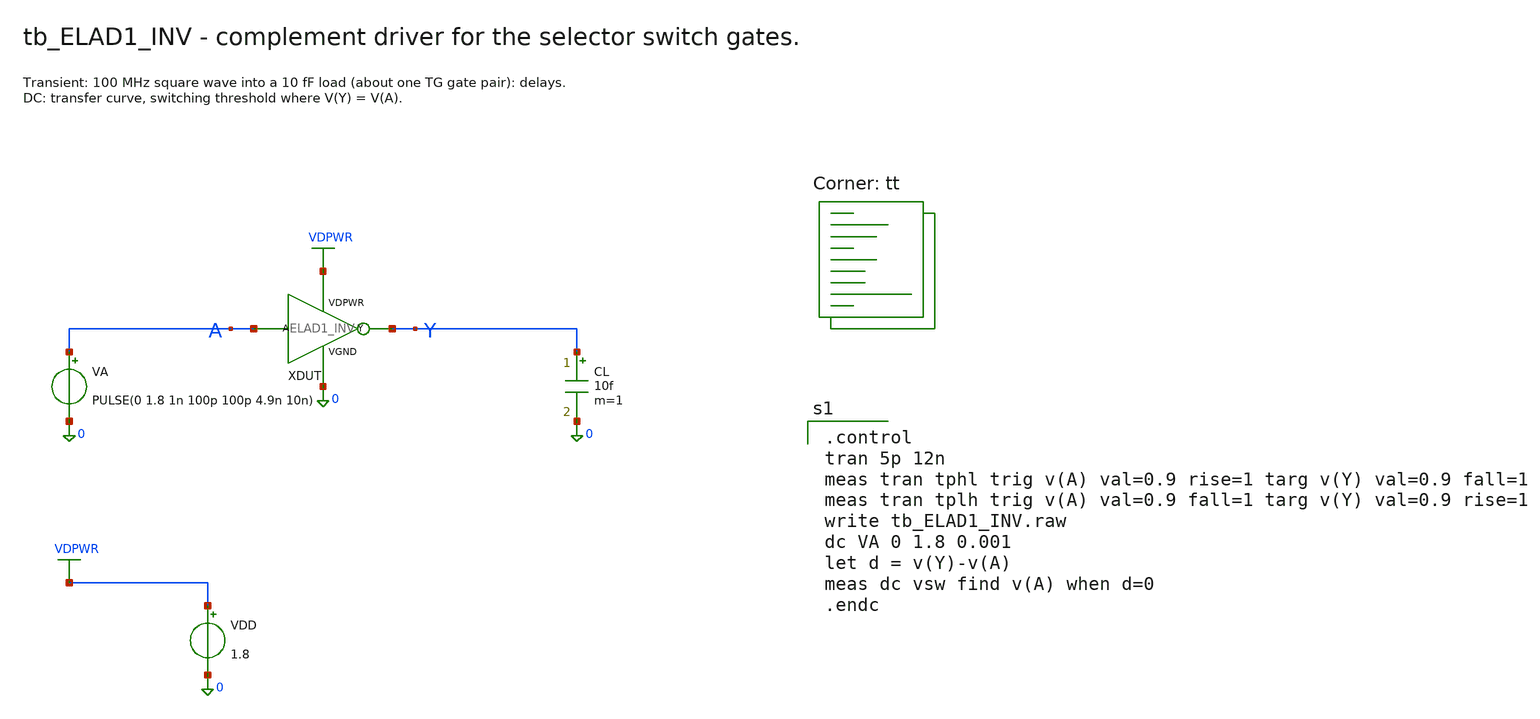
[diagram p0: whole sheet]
** sch_path: cells/ELAD1_INV/schematic/tb_ELAD1_INV.sch
**.subckt tb_ELAD1_INV
XDUT A Y VDPWR 0 ELAD1_INV
VA A 0 PULSE(0 1.8 1n 100p 100p 4.9n 10n)
CL Y 0 10f m=1
VDD VDPWR 0 1.8
**** begin user architecture code

.control
tran 5p 12n
meas tran tphl trig v(A) val=0.9 rise=1 targ v(Y) val=0.9 fall=1
meas tran tplh trig v(A) val=0.9 fall=1 targ v(Y) val=0.9 rise=1
write tb_ELAD1_INV.raw
dc VA 0 1.8 0.001
let d = v(Y)-v(A)
meas dc vsw find v(A) when d=0
.endc

.lib $::SKYWATER_MODELS/sky130.lib.spice tt
**** end user architecture code
**.ends

* expanding   symbol:  ELAD1_INV.sym # of pins=4
** sym_path: cells/ELAD1_INV/schematic/ELAD1_INV.sym
** sch_path: cells/ELAD1_INV/schematic/ELAD1_INV.sch
.subckt ELAD1_INV A Y VDPWR VGND
*.iopin A
*.iopin Y
*.iopin VDPWR
*.iopin VGND
XMN Y A VGND VGND sky130_fd_pr__nfet_01v8 L=0.15 W=0.65 nf=1 ad='int((1 + 1)/2) * 0.65 / 1 * 0.29' as='int((1 + 2)/2) * 0.65 / 1 * 0.29'
+ pd='2*int((1 + 1)/2) * (0.65 / 1 + 0.29)' ps='2*int((1 + 2)/2) * (0.65 / 1 + 0.29)' nrd='0.29 / 0.65 '
+ nrs='0.29 / 0.65 ' sa=0 sb=0 sd=0 mult=1 m=1
XMP Y A VDPWR VDPWR sky130_fd_pr__pfet_01v8 L=0.15 W=1 nf=1 ad='int((nf+1)/2) * W/nf * 0.29' as='int((nf+2)/2) * W/nf * 0.29'
+ pd='2*int((nf+1)/2) * (W/nf + 0.29)' ps='2*int((nf+2)/2) * (W/nf + 0.29)' nrd='0.29 / W' nrs='0.29 / W'
+ sa=0 sb=0 sd=0 mult=1 m=1
.ends

.GLOBAL VGND
.GLOBAL VDPWR
.end
